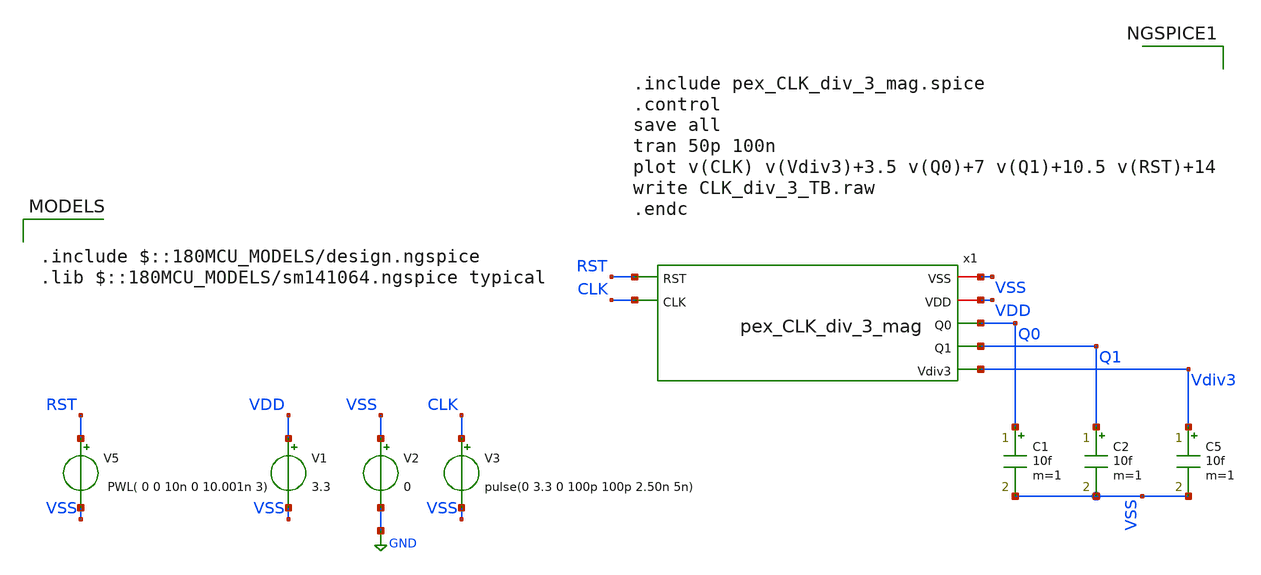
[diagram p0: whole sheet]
** sch_path: Clock_Generator_PAKISTAN_02/xschem/pex_CLK_div_3_TB.sch
**.subckt pex_CLK_div_3_TB
V1 VDD VSS 3.3
V2 VSS GND 0
V3 CLK VSS pulse(0 3.3 0 100p 100p 2.50n 5n)
C1 Q0 VSS 10f m=1
C2 Q1 VSS 10f m=1
C5 Vdiv3 VSS 10f m=1
V5 RST VSS PWL( 0 0 10n 0 10.001n 3)
x1 VSS VDD Q0 Q1 RST Vdiv3 CLK pex_CLK_div_3_mag
**** begin user architecture code

.include $::180MCU_MODELS/design.ngspice
.lib $::180MCU_MODELS/sm141064.ngspice typical



.include pex_CLK_div_3_mag.spice
.control
save all
tran 50p 100n
plot v(CLK) v(Vdiv3)+3.5 v(Q0)+7 v(Q1)+10.5 v(RST)+14
write CLK_div_3_TB.raw
.endc


**** end user architecture code
**.ends
.GLOBAL GND
.end
